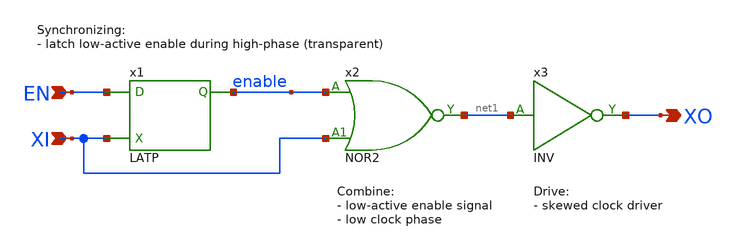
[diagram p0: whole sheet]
** sch_path: Sources/macros/CGN2.sch
**.subckt CGN2 EN XI XO
*.ipin EN
*.ipin XI
*.opin XO
x1 EN XI enable VDD GND LATP Wmin=1.5u Lmin=1u g=2 m=1
x2 enable XI net1 VDD GND NOR2 Wmin=1.5u Lmin=1u g=2 m=1
x3 net1 XO VDD GND INV Wmin=1.5u Lmin=1u g=2 m=1
**.ends
.end
